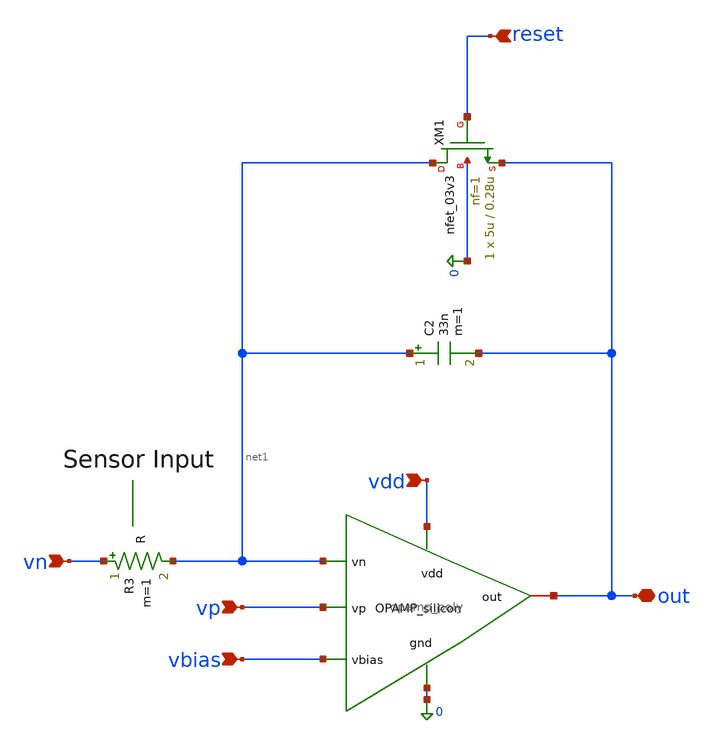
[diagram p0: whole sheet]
** sch_path: xschem/mox_integrator/int.sch
**.subckt int vbias vp vn vdd out reset
*.ipin vbias
*.ipin vp
*.ipin vn
*.ipin vdd
*.iopin out
*.ipin reset
C2 net1 out 33n m=1
XM1 net1 reset out 0 nfet_03v3 L=0.28u W=5u nf=1 ad='int((nf+1)/2) * W/nf * 0.18u' as='int((nf+2)/2) * W/nf * 0.18u'
+ pd='2*int((nf+1)/2) * (W/nf + 0.18u)' ps='2*int((nf+2)/2) * (W/nf + 0.18u)' nrd='0.18u / W' nrs='0.18u / W'
+ sa=0 sb=0 sd=0 m=1
x1 vdd net1 0 out vp vbias opamp_poly
R3 vn net1 R m=1
**.ends

* expanding   symbol:  GF180/xschem/Chipathon/OpAMP_Silicon/opamp_poly.sym # of pins=6
** sym_path: OpAmP/opamp_poly.sym
** sch_path: OpAmP/opamp_poly.sch
.subckt opamp_poly vdd vn gnd out vp vbias
*.ipin gnd
*.iopin out
*.ipin vbias
*.ipin vp
*.ipin vn
*.ipin vdd
XM1 net3 vbias gnd gnd nfet_03v3 L=l1 W=w1 nf=1 ad='int((nf+1)/2) * W/nf * 0.18u' as='int((nf+2)/2) * W/nf * 0.18u'
+ pd='2*int((nf+1)/2) * (W/nf + 0.18u)' ps='2*int((nf+2)/2) * (W/nf + 0.18u)' nrd='0.18u / W' nrs='0.18u / W'
+ sa=0 sb=0 sd=0 m=1
XM2 net2 net2 vdd vdd pfet_03v3 L=l2 W=w2 nf=1 ad='int((nf+1)/2) * W/nf * 0.18u' as='int((nf+2)/2) * W/nf * 0.18u'
+ pd='2*int((nf+1)/2) * (W/nf + 0.18u)' ps='2*int((nf+2)/2) * (W/nf + 0.18u)' nrd='0.18u / W' nrs='0.18u / W'
+ sa=0 sb=0 sd=0 m=1
XM3 out vbias gnd gnd nfet_03v3 L=l3 W=w3 nf=1 ad='int((nf+1)/2) * W/nf * 0.18u' as='int((nf+2)/2) * W/nf * 0.18u'
+ pd='2*int((nf+1)/2) * (W/nf + 0.18u)' ps='2*int((nf+2)/2) * (W/nf + 0.18u)' nrd='0.18u / W' nrs='0.18u / W'
+ sa=0 sb=0 sd=0 m=1
XM4 net2 vn net3 gnd nfet_03v3 L=l4 W=w4 nf=1 ad='int((nf+1)/2) * W/nf * 0.18u' as='int((nf+2)/2) * W/nf * 0.18u'
+ pd='2*int((nf+1)/2) * (W/nf + 0.18u)' ps='2*int((nf+2)/2) * (W/nf + 0.18u)' nrd='0.18u / W' nrs='0.18u / W'
+ sa=0 sb=0 sd=0 m=1
XM5 net1 vp net3 gnd nfet_03v3 L=l5 W=w5 nf=1 ad='int((nf+1)/2) * W/nf * 0.18u' as='int((nf+2)/2) * W/nf * 0.18u'
+ pd='2*int((nf+1)/2) * (W/nf + 0.18u)' ps='2*int((nf+2)/2) * (W/nf + 0.18u)' nrd='0.18u / W' nrs='0.18u / W'
+ sa=0 sb=0 sd=0 m=1
XM6 net1 net2 vdd vdd pfet_03v3 L=l6 W=w6 nf=1 ad='int((nf+1)/2) * W/nf * 0.18u' as='int((nf+2)/2) * W/nf * 0.18u'
+ pd='2*int((nf+1)/2) * (W/nf + 0.18u)' ps='2*int((nf+2)/2) * (W/nf + 0.18u)' nrd='0.18u / W' nrs='0.18u / W'
+ sa=0 sb=0 sd=0 m=1
XM7 out net1 vdd vdd pfet_03v3 L=l7 W=w7 nf=1 ad='int((nf+1)/2) * W/nf * 0.18u' as='int((nf+2)/2) * W/nf * 0.18u'
+ pd='2*int((nf+1)/2) * (W/nf + 0.18u)' ps='2*int((nf+2)/2) * (W/nf + 0.18u)' nrd='0.18u / W' nrs='0.18u / W'
+ sa=0 sb=0 sd=0 m=1
XR1 net4 net1 gnd ppolyf_u_1k r_width=3e-6 r_length=6.6e-6 m=1
XC1 out net4 cap_mim_1f5fF c_width=20e-6 c_length=20e-6 m=1
.ends

.end
